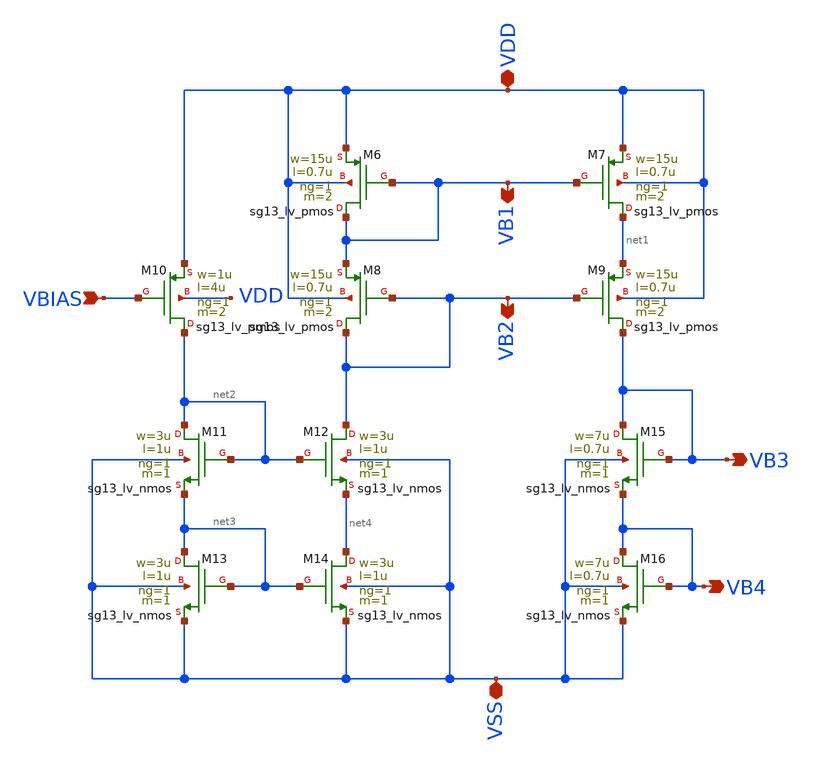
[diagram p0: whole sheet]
** sch_path: BTDay8-Ex/AMP_BIAS_08V.sch
**.subckt AMP_BIAS_08V VDD VSS VBIAS VB1 VB2 VB3 VB4
*.iopin VDD
*.iopin VSS
*.ipin VBIAS
*.opin VB1
*.opin VB2
*.opin VB3
*.opin VB4
XM6 VB1 VB1 VDD VDD sg13_lv_pmos w=15u l=0.7u ng=1 m=2 mm_ok=1
XM7 net1 VB1 VDD VDD sg13_lv_pmos w=15u l=0.7u ng=1 m=2 mm_ok=1
XM9 VB3 VB2 net1 VDD sg13_lv_pmos w=15u l=0.7u ng=1 m=2 mm_ok=1
XM10 net2 VBIAS VDD VDD sg13_lv_pmos w=1u l=4u ng=1 m=2 mm_ok=1
XM11 net2 net2 net3 VSS sg13_lv_nmos w=3u l=1u ng=1 m=1 mm_ok=1
XM12 VB2 net2 net4 VSS sg13_lv_nmos w=3u l=1u ng=1 m=1 mm_ok=1
XM13 net3 net3 VSS VSS sg13_lv_nmos w=3u l=1u ng=1 m=1 mm_ok=1
XM15 VB3 VB3 VB4 VSS sg13_lv_nmos w=7u l=0.7u ng=1 m=1 mm_ok=1
XM16 VB4 VB4 VSS VSS sg13_lv_nmos w=7u l=0.7u ng=1 m=1 mm_ok=1
XM8 VB2 VB2 VB1 VDD sg13_lv_pmos w=15u l=0.7u ng=1 m=2 mm_ok=1
XM14 net4 net3 VSS VSS sg13_lv_nmos w=3u l=1u ng=1 m=1 mm_ok=1
**.ends
.end
